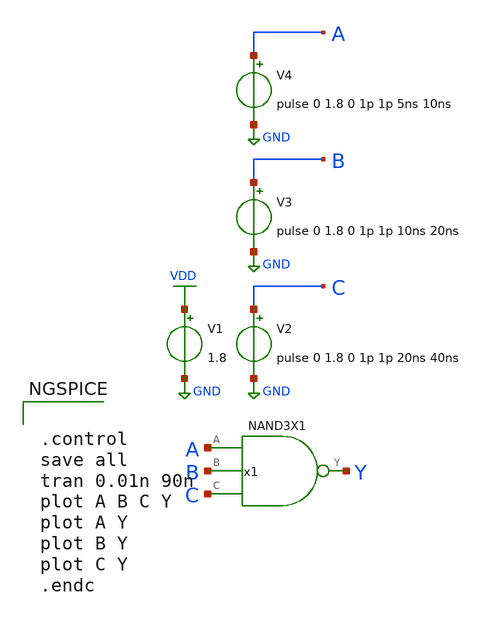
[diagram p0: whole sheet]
** sch_path: lib/xschem/test_NAND3X1.sch
**.subckt test_NAND3X1
V2 C GND pulse 0 1.8 0 1p 1p 20ns 40ns
V1 VDD GND 1.8
V3 B GND pulse 0 1.8 0 1p 1p 10ns 20ns
V4 A GND pulse 0 1.8 0 1p 1p 5ns 10ns
x1 Y A B C NAND3X1
**** begin user architecture code

.lib $::SKYWATER_MODELS/sky130.lib.spice tt


**** end user architecture code
**.ends

* expanding   symbol:  NAND3X1.sym # of pins=4
** sym_path: lib/xschem/NAND3X1.sym
** sch_path: lib/xschem/NAND3X1.sch
.subckt NAND3X1 Y A B C
*.ipin A
*.opin Y
*.ipin B
*.ipin C
XM1 net2 C VSSPIN VSSPIN sky130_fd_pr__nfet_01v8 L=0.15 W=3 nf=1 ad='int((nf+1)/2) * W/nf * 0.29' as='int((nf+2)/2) * W/nf * 0.29'
+ pd='2*int((nf+1)/2) * (W/nf + 0.29)' ps='2*int((nf+2)/2) * (W/nf + 0.29)' nrd='0.29 / W' nrs='0.29 / W'
+ sa=0 sb=0 sd=0 mult=1 m=1
XM2 Y A VCCPIN VCCPIN sky130_fd_pr__pfet_01v8 L=0.15 W=2 nf=1 ad='int((nf+1)/2) * W/nf * 0.29' as='int((nf+2)/2) * W/nf * 0.29'
+ pd='2*int((nf+1)/2) * (W/nf + 0.29)' ps='2*int((nf+2)/2) * (W/nf + 0.29)' nrd='0.29 / W' nrs='0.29 / W'
+ sa=0 sb=0 sd=0 mult=1 m=1
XM3 net1 B net2 VSSPIN sky130_fd_pr__nfet_01v8 L=0.15 W=3 nf=1 ad='int((nf+1)/2) * W/nf * 0.29' as='int((nf+2)/2) * W/nf * 0.29'
+ pd='2*int((nf+1)/2) * (W/nf + 0.29)' ps='2*int((nf+2)/2) * (W/nf + 0.29)' nrd='0.29 / W' nrs='0.29 / W'
+ sa=0 sb=0 sd=0 mult=1 m=1
XM4 Y A net1 VSSPIN sky130_fd_pr__nfet_01v8 L=0.15 W=3 nf=1 ad='int((nf+1)/2) * W/nf * 0.29' as='int((nf+2)/2) * W/nf * 0.29'
+ pd='2*int((nf+1)/2) * (W/nf + 0.29)' ps='2*int((nf+2)/2) * (W/nf + 0.29)' nrd='0.29 / W' nrs='0.29 / W'
+ sa=0 sb=0 sd=0 mult=1 m=1
XM5 Y A VCCPIN VCCPIN sky130_fd_pr__pfet_01v8 L=0.15 W=2 nf=1 ad='int((nf+1)/2) * W/nf * 0.29' as='int((nf+2)/2) * W/nf * 0.29'
+ pd='2*int((nf+1)/2) * (W/nf + 0.29)' ps='2*int((nf+2)/2) * (W/nf + 0.29)' nrd='0.29 / W' nrs='0.29 / W'
+ sa=0 sb=0 sd=0 mult=1 m=1
XM6 Y B VCCPIN VCCPIN sky130_fd_pr__pfet_01v8 L=0.15 W=2 nf=1 ad='int((nf+1)/2) * W/nf * 0.29' as='int((nf+2)/2) * W/nf * 0.29'
+ pd='2*int((nf+1)/2) * (W/nf + 0.29)' ps='2*int((nf+2)/2) * (W/nf + 0.29)' nrd='0.29 / W' nrs='0.29 / W'
+ sa=0 sb=0 sd=0 mult=1 m=1
XM7 Y B VCCPIN VCCPIN sky130_fd_pr__pfet_01v8 L=0.15 W=2 nf=1 ad='int((nf+1)/2) * W/nf * 0.29' as='int((nf+2)/2) * W/nf * 0.29'
+ pd='2*int((nf+1)/2) * (W/nf + 0.29)' ps='2*int((nf+2)/2) * (W/nf + 0.29)' nrd='0.29 / W' nrs='0.29 / W'
+ sa=0 sb=0 sd=0 mult=1 m=1
XM8 Y C VCCPIN VCCPIN sky130_fd_pr__pfet_01v8 L=0.15 W=2 nf=1 ad='int((nf+1)/2) * W/nf * 0.29' as='int((nf+2)/2) * W/nf * 0.29'
+ pd='2*int((nf+1)/2) * (W/nf + 0.29)' ps='2*int((nf+2)/2) * (W/nf + 0.29)' nrd='0.29 / W' nrs='0.29 / W'
+ sa=0 sb=0 sd=0 mult=1 m=1
XM9 Y C VCCPIN VCCPIN sky130_fd_pr__pfet_01v8 L=0.15 W=2 nf=1 ad='int((nf+1)/2) * W/nf * 0.29' as='int((nf+2)/2) * W/nf * 0.29'
+ pd='2*int((nf+1)/2) * (W/nf + 0.29)' ps='2*int((nf+2)/2) * (W/nf + 0.29)' nrd='0.29 / W' nrs='0.29 / W'
+ sa=0 sb=0 sd=0 mult=1 m=1
.ends

.GLOBAL VDD
.GLOBAL GND
**** begin user architecture code


.control
save all
tran 0.01n 90n
plot A B C Y
plot A Y
plot B Y
plot C Y
.endc


**** end user architecture code
.end
